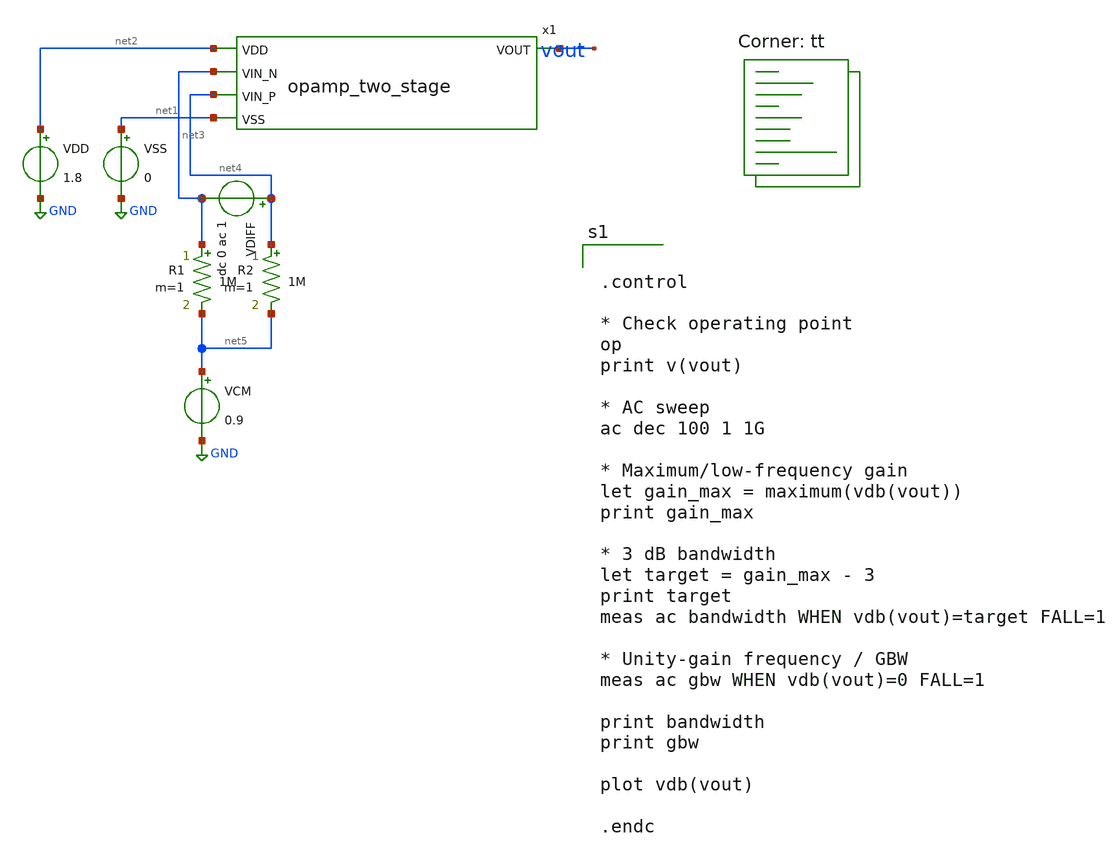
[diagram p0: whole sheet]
** sch_path: analog/build/schematic/tb_ac_analysis.sch
**.subckt tb_ac_analysis
VSS net1 GND 0
VDD net2 GND 1.8
VDIFF net4 net3 dc 0 ac 1
R1 net3 net5 1M m=1
R2 net4 net5 1M m=1
VCM net5 GND 0.9
x1 net2 vout net3 net4 net1 opamp_two_stage
**** begin user architecture code
.lib $::SKYWATER_MODELS/sky130.lib.spice tt


.control

* Check operating point
op
print v(vout)

* AC sweep
ac dec 100 1 1G

* Maximum/low-frequency gain
let gain_max = maximum(vdb(vout))
print gain_max

* 3 dB bandwidth
let target = gain_max - 3
print target
meas ac bandwidth WHEN vdb(vout)=target FALL=1

* Unity-gain frequency / GBW
meas ac gbw WHEN vdb(vout)=0 FALL=1

print bandwidth
print gbw

plot vdb(vout)

.endc


**** end user architecture code
**.ends

* expanding   symbol:  opamp_two_stage.sym # of pins=5
** sym_path: analog/build/schematic/opamp_two_stage.sym
** sch_path: analog/build/schematic/opamp_two_stage.sch
.subckt opamp_two_stage VDD VOUT VIN_N VIN_P VSS
*.ipin VIN_N
*.ipin VIN_P
*.opin VOUT
*.ipin VDD
*.ipin VSS
XM1 net3 VIN_N net1 VSS sky130_fd_pr__nfet_01v8 L=1 W=10 nf=1 ad='int((nf+1)/2) * W/nf * 0.29' as='int((nf+2)/2) * W/nf * 0.29'
+ pd='2*int((nf+1)/2) * (W/nf + 0.29)' ps='2*int((nf+2)/2) * (W/nf + 0.29)' nrd='0.29 / W' nrs='0.29 / W'
+ sa=0 sb=0 sd=0 mult=1 m=1
XM2 net2 VIN_P net1 VSS sky130_fd_pr__nfet_01v8 L=1 W=10 nf=1 ad='int((nf+1)/2) * W/nf * 0.29' as='int((nf+2)/2) * W/nf * 0.29'
+ pd='2*int((nf+1)/2) * (W/nf + 0.29)' ps='2*int((nf+2)/2) * (W/nf + 0.29)' nrd='0.29 / W' nrs='0.29 / W'
+ sa=0 sb=0 sd=0 mult=1 m=1
XM3 net1 net5 VSS VSS sky130_fd_pr__nfet_01v8 L=2 W=10 nf=1 ad='int((nf+1)/2) * W/nf * 0.29' as='int((nf+2)/2) * W/nf * 0.29'
+ pd='2*int((nf+1)/2) * (W/nf + 0.29)' ps='2*int((nf+2)/2) * (W/nf + 0.29)' nrd='0.29 / W' nrs='0.29 / W'
+ sa=0 sb=0 sd=0 mult=1 m=1
XM4 net3 net2 VDD VDD sky130_fd_pr__pfet_01v8 L=1 W=20 nf=1 ad='int((nf+1)/2) * W/nf * 0.29' as='int((nf+2)/2) * W/nf * 0.29'
+ pd='2*int((nf+1)/2) * (W/nf + 0.29)' ps='2*int((nf+2)/2) * (W/nf + 0.29)' nrd='0.29 / W' nrs='0.29 / W'
+ sa=0 sb=0 sd=0 mult=1 m=1
XM5 net2 net2 VDD VDD sky130_fd_pr__pfet_01v8 L=1 W=20 nf=1 ad='int((nf+1)/2) * W/nf * 0.29' as='int((nf+2)/2) * W/nf * 0.29'
+ pd='2*int((nf+1)/2) * (W/nf + 0.29)' ps='2*int((nf+2)/2) * (W/nf + 0.29)' nrd='0.29 / W' nrs='0.29 / W'
+ sa=0 sb=0 sd=0 mult=1 m=1
XM7 VOUT net5 VSS VSS sky130_fd_pr__nfet_01v8 L=2 W=10 nf=1 ad='int((nf+1)/2) * W/nf * 0.29' as='int((nf+2)/2) * W/nf * 0.29'
+ pd='2*int((nf+1)/2) * (W/nf + 0.29)' ps='2*int((nf+2)/2) * (W/nf + 0.29)' nrd='0.29 / W' nrs='0.29 / W'
+ sa=0 sb=0 sd=0 mult=1 m=1
XM8 VOUT net3 VDD VDD sky130_fd_pr__pfet_01v8 L=1 W=20 nf=1 ad='int((nf+1)/2) * W/nf * 0.29' as='int((nf+2)/2) * W/nf * 0.29'
+ pd='2*int((nf+1)/2) * (W/nf + 0.29)' ps='2*int((nf+2)/2) * (W/nf + 0.29)' nrd='0.29 / W' nrs='0.29 / W'
+ sa=0 sb=0 sd=0 mult=1 m=1
C1 net3 net4 1p m=1
R1 VOUT net4 2k m=1
XM_bias net5 net5 VSS VSS sky130_fd_pr__nfet_01v8 L=2 W=10 nf=1 ad='int((nf+1)/2) * W/nf * 0.29' as='int((nf+2)/2) * W/nf * 0.29'
+ pd='2*int((nf+1)/2) * (W/nf + 0.29)' ps='2*int((nf+2)/2) * (W/nf + 0.29)' nrd='0.29 / W' nrs='0.29 / W'
+ sa=0 sb=0 sd=0 mult=1 m=1
R2 VDD net5 10k m=1
.ends

.GLOBAL GND
.end
